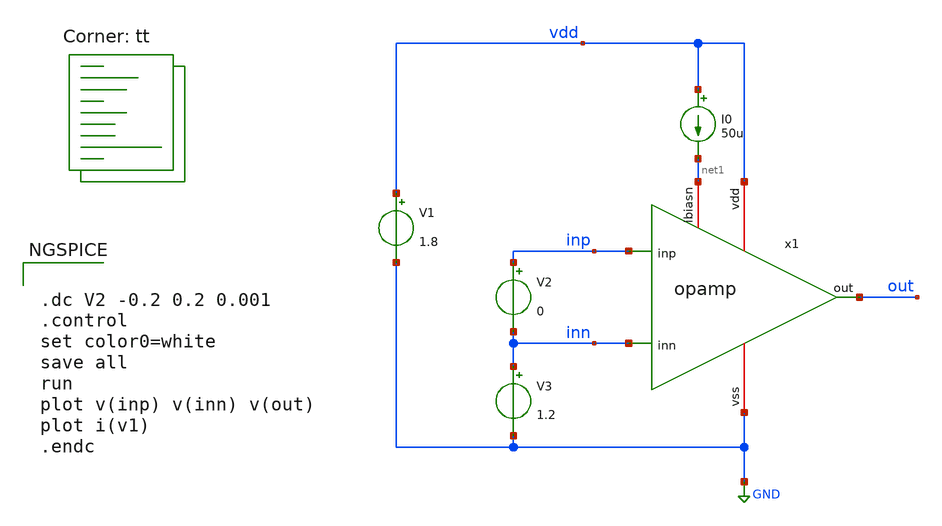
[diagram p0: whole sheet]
** sch_path: sky130A/HelloWorld/xschem/tb_opamp_0.sch
**.subckt tb_opamp_0
x1 vdd out inp inn net1 GND opamp
V1 vdd GND 1.8
I0 vdd net1 50u
V2 inp inn 0
V3 inn GND 1.2
**** begin user architecture code
.lib $::SKYWATER_MODELS/sky130.lib.spice tt


.dc V2 -0.2 0.2 0.001
.control
set color0=white
save all
run
plot v(inp) v(inn) v(out)
plot i(v1)
.endc


**** end user architecture code
**.ends

* expanding   symbol:  opamp.sym # of pins=6
** sym_path: sky130A/HelloWorld/xschem/opamp.sym
** sch_path: sky130A/HelloWorld/xschem/opamp.sch
.subckt opamp vdd out inp inn ibiasn vss
*.ipin inn
*.ipin inp
*.iopin vdd
*.iopin vss
*.iopin ibiasn
*.opin out
XM1 pbias inn tail vss sky130_fd_pr__nfet_01v8 L=1 W=40 nf=1 ad='int((nf+1)/2) * W/nf * 0.29' as='int((nf+2)/2) * W/nf * 0.29'
+ pd='2*int((nf+1)/2) * (W/nf + 0.29)' ps='2*int((nf+2)/2) * (W/nf + 0.29)' nrd='0.29 / W' nrs='0.29 / W'
+ sa=0 sb=0 sd=0 mult=1 m=1
XM2 outz inp tail vss sky130_fd_pr__nfet_01v8 L=1 W=40 nf=1 ad='int((nf+1)/2) * W/nf * 0.29' as='int((nf+2)/2) * W/nf * 0.29'
+ pd='2*int((nf+1)/2) * (W/nf + 0.29)' ps='2*int((nf+2)/2) * (W/nf + 0.29)' nrd='0.29 / W' nrs='0.29 / W'
+ sa=0 sb=0 sd=0 mult=1 m=1
XM3 pbias pbias vdd vdd sky130_fd_pr__pfet_01v8 L=0.5 W=20 nf=1 ad='int((nf+1)/2) * W/nf * 0.29' as='int((nf+2)/2) * W/nf * 0.29'
+ pd='2*int((nf+1)/2) * (W/nf + 0.29)' ps='2*int((nf+2)/2) * (W/nf + 0.29)' nrd='0.29 / W' nrs='0.29 / W'
+ sa=0 sb=0 sd=0 mult=1 m=1
XM4 outz pbias vdd vdd sky130_fd_pr__pfet_01v8 L=0.5 W=20 nf=1 ad='int((nf+1)/2) * W/nf * 0.29' as='int((nf+2)/2) * W/nf * 0.29'
+ pd='2*int((nf+1)/2) * (W/nf + 0.29)' ps='2*int((nf+2)/2) * (W/nf + 0.29)' nrd='0.29 / W' nrs='0.29 / W'
+ sa=0 sb=0 sd=0 mult=1 m=1
XM5 out outz vdd vdd sky130_fd_pr__pfet_01v8 L=0.5 W=20 nf=1 ad='int((nf+1)/2) * W/nf * 0.29' as='int((nf+2)/2) * W/nf * 0.29'
+ pd='2*int((nf+1)/2) * (W/nf + 0.29)' ps='2*int((nf+2)/2) * (W/nf + 0.29)' nrd='0.29 / W' nrs='0.29 / W'
+ sa=0 sb=0 sd=0 mult=1 m=1
XM6[1] tail ibiasn vss vss sky130_fd_pr__nfet_01v8 L=1 W=40 nf=1 ad='int((nf+1)/2) * W/nf * 0.29' as='int((nf+2)/2) * W/nf * 0.29'
+ pd='2*int((nf+1)/2) * (W/nf + 0.29)' ps='2*int((nf+2)/2) * (W/nf + 0.29)' nrd='0.29 / W' nrs='0.29 / W'
+ sa=0 sb=0 sd=0 mult=1 m=1
XM6[0] tail ibiasn vss vss sky130_fd_pr__nfet_01v8 L=1 W=40 nf=1 ad='int((nf+1)/2) * W/nf * 0.29' as='int((nf+2)/2) * W/nf * 0.29'
+ pd='2*int((nf+1)/2) * (W/nf + 0.29)' ps='2*int((nf+2)/2) * (W/nf + 0.29)' nrd='0.29 / W' nrs='0.29 / W'
+ sa=0 sb=0 sd=0 mult=1 m=1
XM7 out ibiasn vss vss sky130_fd_pr__nfet_01v8 L=1 W=40 nf=1 ad='int((nf+1)/2) * W/nf * 0.29' as='int((nf+2)/2) * W/nf * 0.29'
+ pd='2*int((nf+1)/2) * (W/nf + 0.29)' ps='2*int((nf+2)/2) * (W/nf + 0.29)' nrd='0.29 / W' nrs='0.29 / W'
+ sa=0 sb=0 sd=0 mult=1 m=1
XM8 ibiasn ibiasn vss vss sky130_fd_pr__nfet_01v8 L=1 W=40 nf=1 ad='int((nf+1)/2) * W/nf * 0.29' as='int((nf+2)/2) * W/nf * 0.29'
+ pd='2*int((nf+1)/2) * (W/nf + 0.29)' ps='2*int((nf+2)/2) * (W/nf + 0.29)' nrd='0.29 / W' nrs='0.29 / W'
+ sa=0 sb=0 sd=0 mult=1 m=1
.ends

.GLOBAL GND
.end
